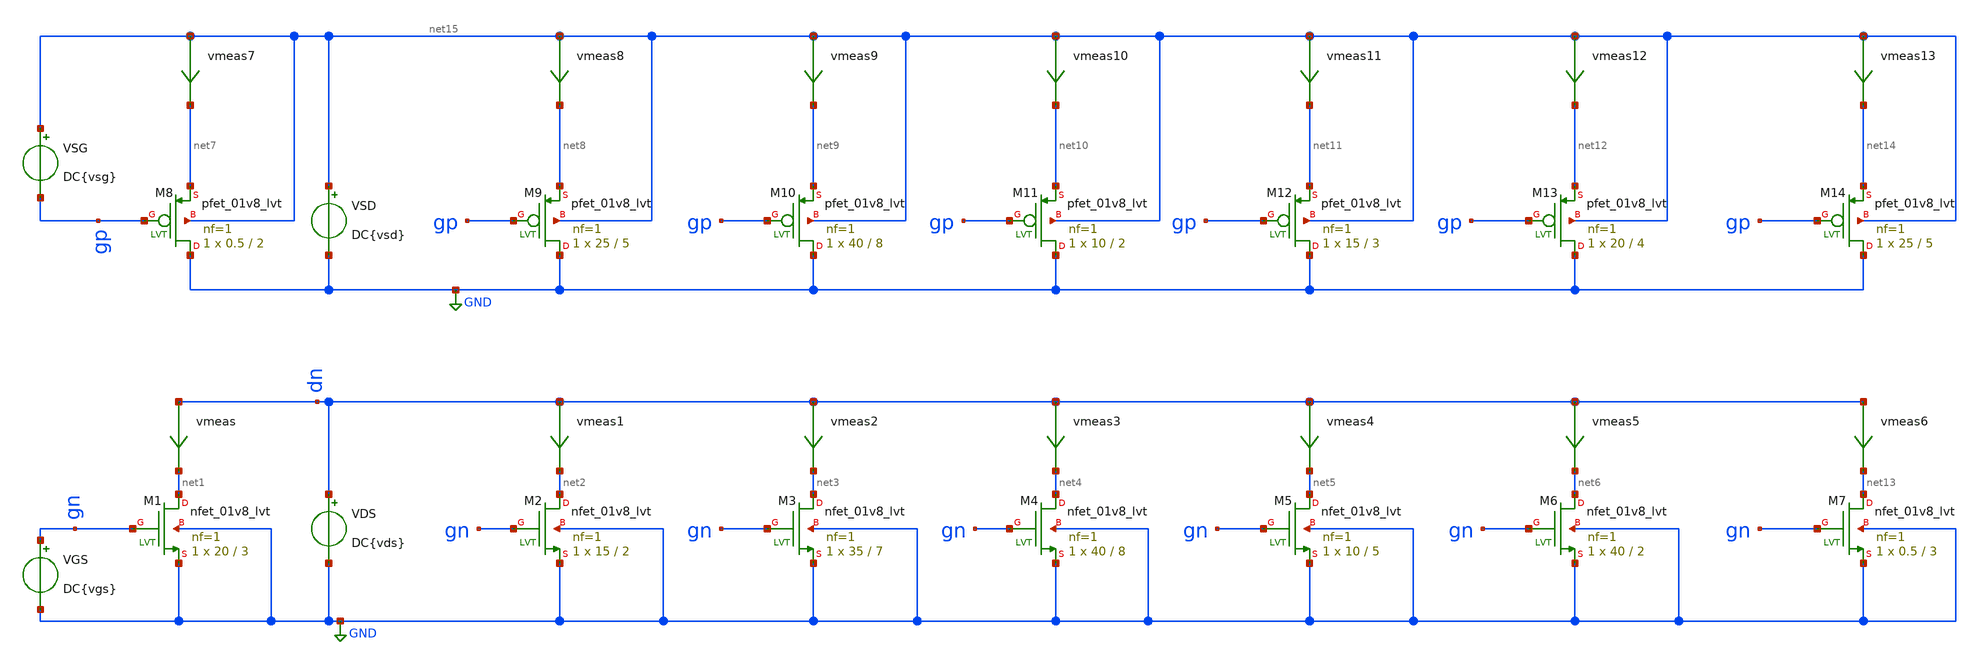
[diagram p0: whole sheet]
** sch_path: XSCHEM/r0_characterization_lvt_01v8.sch
**.subckt r0_characterization_lvt_01v8
XM1 net1 gn GND GND sky130_fd_pr__nfet_01v8_lvt L=3 W=20 nf=1 ad='int((nf+1)/2) * W/nf * 0.29' as='int((nf+2)/2) * W/nf * 0.29'
+ pd='2*int((nf+1)/2) * (W/nf + 0.29)' ps='2*int((nf+2)/2) * (W/nf + 0.29)' nrd='0.29 / W' nrs='0.29 / W'
+ sa=0 sb=0 sd=0 mult=1 m=1
XM2 net2 gn GND GND sky130_fd_pr__nfet_01v8_lvt L=2 W=15 nf=1 ad='int((nf+1)/2) * W/nf * 0.29' as='int((nf+2)/2) * W/nf * 0.29'
+ pd='2*int((nf+1)/2) * (W/nf + 0.29)' ps='2*int((nf+2)/2) * (W/nf + 0.29)' nrd='0.29 / W' nrs='0.29 / W'
+ sa=0 sb=0 sd=0 mult=1 m=1
VGS gn GND DC{vgs}
VDS dn GND DC{vds}
XM3 net3 gn GND GND sky130_fd_pr__nfet_01v8_lvt L=7 W=35 nf=1 ad='int((nf+1)/2) * W/nf * 0.29' as='int((nf+2)/2) * W/nf * 0.29'
+ pd='2*int((nf+1)/2) * (W/nf + 0.29)' ps='2*int((nf+2)/2) * (W/nf + 0.29)' nrd='0.29 / W' nrs='0.29 / W'
+ sa=0 sb=0 sd=0 mult=1 m=1
XM4 net4 gn GND GND sky130_fd_pr__nfet_01v8_lvt L=8 W=40 nf=1 ad='int((nf+1)/2) * W/nf * 0.29' as='int((nf+2)/2) * W/nf * 0.29'
+ pd='2*int((nf+1)/2) * (W/nf + 0.29)' ps='2*int((nf+2)/2) * (W/nf + 0.29)' nrd='0.29 / W' nrs='0.29 / W'
+ sa=0 sb=0 sd=0 mult=1 m=1
XM5 net5 gn GND GND sky130_fd_pr__nfet_01v8_lvt L=5 W=10 nf=1 ad='int((nf+1)/2) * W/nf * 0.29' as='int((nf+2)/2) * W/nf * 0.29'
+ pd='2*int((nf+1)/2) * (W/nf + 0.29)' ps='2*int((nf+2)/2) * (W/nf + 0.29)' nrd='0.29 / W' nrs='0.29 / W'
+ sa=0 sb=0 sd=0 mult=1 m=1
XM6 net6 gn GND GND sky130_fd_pr__nfet_01v8_lvt L=2 W=40 nf=1 ad='int((nf+1)/2) * W/nf * 0.29' as='int((nf+2)/2) * W/nf * 0.29'
+ pd='2*int((nf+1)/2) * (W/nf + 0.29)' ps='2*int((nf+2)/2) * (W/nf + 0.29)' nrd='0.29 / W' nrs='0.29 / W'
+ sa=0 sb=0 sd=0 mult=1 m=1
VSG net15 gp DC{vsg}
VSD net15 GND DC{vsd}
XM7 net13 gn GND GND sky130_fd_pr__nfet_01v8_lvt L=3 W=0.5 nf=1 ad='int((nf+1)/2) * W/nf * 0.29' as='int((nf+2)/2) * W/nf * 0.29'
+ pd='2*int((nf+1)/2) * (W/nf + 0.29)' ps='2*int((nf+2)/2) * (W/nf + 0.29)' nrd='0.29 / W' nrs='0.29 / W'
+ sa=0 sb=0 sd=0 mult=1 m=1
XM8 GND gp net7 net15 sky130_fd_pr__pfet_01v8_lvt L=2 W=0.5 nf=1 ad='int((nf+1)/2) * W/nf * 0.29' as='int((nf+2)/2) * W/nf * 0.29'
+ pd='2*int((nf+1)/2) * (W/nf + 0.29)' ps='2*int((nf+2)/2) * (W/nf + 0.29)' nrd='0.29 / W' nrs='0.29 / W'
+ sa=0 sb=0 sd=0 mult=1 m=1
XM9 GND gp net8 net15 sky130_fd_pr__pfet_01v8_lvt L=5 W=25 nf=1 ad='int((nf+1)/2) * W/nf * 0.29' as='int((nf+2)/2) * W/nf * 0.29'
+ pd='2*int((nf+1)/2) * (W/nf + 0.29)' ps='2*int((nf+2)/2) * (W/nf + 0.29)' nrd='0.29 / W' nrs='0.29 / W'
+ sa=0 sb=0 sd=0 mult=1 m=1
XM10 GND gp net9 net15 sky130_fd_pr__pfet_01v8_lvt L=8 W=40 nf=1 ad='int((nf+1)/2) * W/nf * 0.29' as='int((nf+2)/2) * W/nf * 0.29'
+ pd='2*int((nf+1)/2) * (W/nf + 0.29)' ps='2*int((nf+2)/2) * (W/nf + 0.29)' nrd='0.29 / W' nrs='0.29 / W'
+ sa=0 sb=0 sd=0 mult=1 m=1
XM11 GND gp net10 net15 sky130_fd_pr__pfet_01v8_lvt L=2 W=10 nf=1 ad='int((nf+1)/2) * W/nf * 0.29' as='int((nf+2)/2) * W/nf * 0.29'
+ pd='2*int((nf+1)/2) * (W/nf + 0.29)' ps='2*int((nf+2)/2) * (W/nf + 0.29)' nrd='0.29 / W' nrs='0.29 / W'
+ sa=0 sb=0 sd=0 mult=1 m=1
XM12 GND gp net11 net15 sky130_fd_pr__pfet_01v8_lvt L=3 W=15 nf=1 ad='int((nf+1)/2) * W/nf * 0.29' as='int((nf+2)/2) * W/nf * 0.29'
+ pd='2*int((nf+1)/2) * (W/nf + 0.29)' ps='2*int((nf+2)/2) * (W/nf + 0.29)' nrd='0.29 / W' nrs='0.29 / W'
+ sa=0 sb=0 sd=0 mult=1 m=1
XM13 GND gp net12 net15 sky130_fd_pr__pfet_01v8_lvt L=4 W=20 nf=1 ad='int((nf+1)/2) * W/nf * 0.29' as='int((nf+2)/2) * W/nf * 0.29'
+ pd='2*int((nf+1)/2) * (W/nf + 0.29)' ps='2*int((nf+2)/2) * (W/nf + 0.29)' nrd='0.29 / W' nrs='0.29 / W'
+ sa=0 sb=0 sd=0 mult=1 m=1
XM14 GND gp net14 net15 sky130_fd_pr__pfet_01v8_lvt L=5 W=25 nf=1 ad='int((nf+1)/2) * W/nf * 0.29' as='int((nf+2)/2) * W/nf * 0.29'
+ pd='2*int((nf+1)/2) * (W/nf + 0.29)' ps='2*int((nf+2)/2) * (W/nf + 0.29)' nrd='0.29 / W' nrs='0.29 / W'
+ sa=0 sb=0 sd=0 mult=1 m=1
vmeas dn net1 0
.save i(vmeas)
vmeas1 dn net2 0
.save i(vmeas1)
vmeas2 dn net3 0
.save i(vmeas2)
vmeas3 dn net4 0
.save i(vmeas3)
vmeas4 dn net5 0
.save i(vmeas4)
vmeas5 dn net6 0
.save i(vmeas5)
vmeas6 dn net13 0
.save i(vmeas6)
vmeas7 net15 net7 0
.save i(vmeas7)
vmeas8 net15 net8 0
.save i(vmeas8)
vmeas9 net15 net9 0
.save i(vmeas9)
vmeas10 net15 net10 0
.save i(vmeas10)
vmeas11 net15 net11 0
.save i(vmeas11)
vmeas12 net15 net12 0
.save i(vmeas12)
vmeas13 net15 net14 0
.save i(vmeas13)
**** begin user architecture code



* Parameters
.param vds = 1.8
.param vgs = 0.9
.param vsd = 1.8
.param vsg = 0.9
.options TEMPS = 27.0

* Models
.lib /home/karlajcm/skywater130/skywater-pdk/libraries/sky130_fd_pr/latest/models/sky130.lib.spice TT

* Data to save
.save all  @M.XM1.msky130_fd_pr__nfet_01v8_lvt[id]  @M.XM1.msky130_fd_pr__nfet_01v8_lvt[gm]  @M.XM1.msky130_fd_pr__nfet_01v8_lvt[vth]  @M.XM1.msky130_fd_pr__nfet_01v8_lvt[vds]  @M.XM1.msky130_fd_pr__nfet_01v8_lvt[vdsat]  @M.XM1.msky130_fd_pr__nfet_01v8_lvt[vgs]  @M.XM1.msky130_fd_pr__nfet_01v8_lvt[cgg]  @M.XM2.msky130_fd_pr__nfet_01v8_lvt[id]  @M.XM2.msky130_fd_pr__nfet_01v8_lvt[gm]  @M.XM2.msky130_fd_pr__nfet_01v8_lvt[vth]  @M.XM2.msky130_fd_pr__nfet_01v8_lvt[vds]  @M.XM2.msky130_fd_pr__nfet_01v8_lvt[vdsat]  @M.XM2.msky130_fd_pr__nfet_01v8_lvt[vgs]  @M.XM2.msky130_fd_pr__nfet_01v8_lvt[cgg]  @M.XM3.msky130_fd_pr__nfet_01v8_lvt[id]  @M.XM3.msky130_fd_pr__nfet_01v8_lvt[gm]  @M.XM3.msky130_fd_pr__nfet_01v8_lvt[vth]  @M.XM3.msky130_fd_pr__nfet_01v8_lvt[vds]  @M.XM3.msky130_fd_pr__nfet_01v8_lvt[vdsat]  @M.XM3.msky130_fd_pr__nfet_01v8_lvt[vgs]  @M.XM3.msky130_fd_pr__nfet_01v8_lvt[cgg]  @M.XM4.msky130_fd_pr__nfet_01v8_lvt[id]  @M.XM4.msky130_fd_pr__nfet_01v8_lvt[gm]  @M.XM4.msky130_fd_pr__nfet_01v8_lvt[vth]  @M.XM4.msky130_fd_pr__nfet_01v8_lvt[vds]  @M.XM4.msky130_fd_pr__nfet_01v8_lvt[vdsat]  @M.XM4.msky130_fd_pr__nfet_01v8_lvt[vgs]  @M.XM4.msky130_fd_pr__nfet_01v8_lvt[cgg]  @M.XM5.msky130_fd_pr__nfet_01v8_lvt[id]  @M.XM5.msky130_fd_pr__nfet_01v8_lvt[gm]  @M.XM5.msky130_fd_pr__nfet_01v8_lvt[vth]  @M.XM5.msky130_fd_pr__nfet_01v8_lvt[vds]  @M.XM5.msky130_fd_pr__nfet_01v8_lvt[vdsat]  @M.XM5.msky130_fd_pr__nfet_01v8_lvt[vgs]  @M.XM5.msky130_fd_pr__nfet_01v8_lvt[cgg]  @M.XM6.msky130_fd_pr__nfet_01v8_lvt[id]  @M.XM6.msky130_fd_pr__nfet_01v8_lvt[gm]  @M.XM6.msky130_fd_pr__nfet_01v8_lvt[vth]  @M.XM6.msky130_fd_pr__nfet_01v8_lvt[vds]  @M.XM6.msky130_fd_pr__nfet_01v8_lvt[vdsat]  @M.XM6.msky130_fd_pr__nfet_01v8_lvt[vgs]  @M.XM6.msky130_fd_pr__nfet_01v8_lvt[cgg]  @M.XM7.msky130_fd_pr__nfet_01v8_lvt[id]  @M.XM7.msky130_fd_pr__nfet_01v8_lvt[gm]  @M.XM7.msky130_fd_pr__nfet_01v8_lvt[vth]  @M.XM7.msky130_fd_pr__nfet_01v8_lvt[vds]  @M.XM7.msky130_fd_pr__nfet_01v8_lvt[vdsat]  @M.XM7.msky130_fd_pr__nfet_01v8_lvt[vgs]  @M.XM7.msky130_fd_pr__nfet_01v8_lvt[cgg]  @M.XM8.msky130_fd_pr__pfet_01v8_lvt[id]  @M.XM8.msky130_fd_pr__pfet_01v8_lvt[gm]  @M.XM8.msky130_fd_pr__pfet_01v8_lvt[vth]  @M.XM8.msky130_fd_pr__pfet_01v8_lvt[vds]  @M.XM8.msky130_fd_pr__pfet_01v8_lvt[vdsat]  @M.XM8.msky130_fd_pr__pfet_01v8_lvt[vgs]  @M.XM8.msky130_fd_pr__pfet_01v8_lvt[cgg]  @M.XM9.msky130_fd_pr__pfet_01v8_lvt[id]  @M.XM9.msky130_fd_pr__pfet_01v8_lvt[gm]  @M.XM9.msky130_fd_pr__pfet_01v8_lvt[vth]  @M.XM9.msky130_fd_pr__pfet_01v8_lvt[vds]  @M.XM9.msky130_fd_pr__pfet_01v8_lvt[vdsat]  @M.XM9.msky130_fd_pr__pfet_01v8_lvt[vgs]  @M.XM9.msky130_fd_pr__pfet_01v8_lvt[cgg]  @M.XM10.msky130_fd_pr__pfet_01v8_lvt[id]  @M.XM10.msky130_fd_pr__pfet_01v8_lvt[gm]  @M.XM10.msky130_fd_pr__pfet_01v8_lvt[vth]  @M.XM10.msky130_fd_pr__pfet_01v8_lvt[vds]  @M.XM10.msky130_fd_pr__pfet_01v8_lvt[vdsat]  @M.XM10.msky130_fd_pr__pfet_01v8_lvt[vgs]  @M.XM10.msky130_fd_pr__pfet_01v8_lvt[cgg]  @M.XM11.msky130_fd_pr__pfet_01v8_lvt[id]  @M.XM11.msky130_fd_pr__pfet_01v8_lvt[gm]  @M.XM11.msky130_fd_pr__pfet_01v8_lvt[vth]  @M.XM11.msky130_fd_pr__pfet_01v8_lvt[vds]  @M.XM11.msky130_fd_pr__pfet_01v8_lvt[vdsat]  @M.XM11.msky130_fd_pr__pfet_01v8_lvt[vgs]  @M.XM11.msky130_fd_pr__pfet_01v8_lvt[cgg]  @M.XM12.msky130_fd_pr__pfet_01v8_lvt[id]  @M.XM12.msky130_fd_pr__pfet_01v8_lvt[gm]  @M.XM12.msky130_fd_pr__pfet_01v8_lvt[vth]  @M.XM12.msky130_fd_pr__pfet_01v8_lvt[vds]  @M.XM12.msky130_fd_pr__pfet_01v8_lvt[vdsat]  @M.XM12.msky130_fd_pr__pfet_01v8_lvt[vgs]  @M.XM12.msky130_fd_pr__pfet_01v8_lvt[cgg]  @M.XM13.msky130_fd_pr__pfet_01v8_lvt[id]  @M.XM13.msky130_fd_pr__pfet_01v8_lvt[gm]  @M.XM13.msky130_fd_pr__pfet_01v8_lvt[vth]  @M.XM13.msky130_fd_pr__pfet_01v8_lvt[vds]  @M.XM13.msky130_fd_pr__pfet_01v8_lvt[vdsat]  @M.XM13.msky130_fd_pr__pfet_01v8_lvt[vgs]  @M.XM13.msky130_fd_pr__pfet_01v8_lvt[cgg]  @M.XM14.msky130_fd_pr__pfet_01v8_lvt[id]  @M.XM14.msky130_fd_pr__pfet_01v8_lvt[gm]  @M.XM14.msky130_fd_pr__pfet_01v8_lvt[vth]  @M.XM14.msky130_fd_pr__pfet_01v8_lvt[vds]  @M.XM14.msky130_fd_pr__pfet_01v8_lvt[vdsat]  @M.XM14.msky130_fd_pr__pfet_01v8_lvt[vgs]  @M.XM14.msky130_fd_pr__pfet_01v8_lvt[cgg]

* Simulation
.control
  dc VDS 0 1.8 0.01 VGS 0 1.8 0.3 VSD 0 1.8 0.01 VSG 0 1.8 0.3
  setplot dc1
  plot @M.XM1.msky130_fd_pr__nfet_01v8_lvt[id] @M.XM2.msky130_fd_pr__nfet_01v8_lvt[id] @M.XM3.msky130_fd_pr__nfet_01v8_lvt[id]
+ @M.XM4.msky130_fd_pr__nfet_01v8_lvt[id] @M.XM5.msky130_fd_pr__nfet_01v8_lvt[id] @M.XM6.msky130_fd_pr__nfet_01v8_lvt[id]
+ @M.XM7.msky130_fd_pr__nfet_01v8_lvt[id] ylabel Id xlabel Vds title 'NMOS: Id vs Vds vs Vgs'
  plot @M.XM8.msky130_fd_pr__pfet_01v8_lvt[id] @M.XM9.msky130_fd_pr__pfet_01v8_lvt[id] @M.XM10.msky130_fd_pr__pfet_01v8_lvt[id]
+ @M.XM11.msky130_fd_pr__pfet_01v8_lvt[id] @M.XM12.msky130_fd_pr__pfet_01v8_lvt[id] @M.XM13.msky130_fd_pr__pfet_01v8_lvt[id]
+ @M.XM14.msky130_fd_pr__pfet_01v8_lvt[id] ylabel Id xlabel Vsd title 'PMOS:Id vs Vsd vs Vsg'
  set filetype = ascii
  write r0_characterization_lvt_01v8_dc1.raw

  reset
  dc VDS 0 1.8 0.01
  setplot dc2
  plot i(vmeas) ylabel Ids xlabel Vds title 'M1:NMOS:Ids vs Vds'
  plot i(vmeas1) ylabel Ids xlabel Vds title 'M2:NMOS:Ids vs Vds'
  plot i(vmeas2) ylabel Ids xlabel Vds title 'M3:NMOS:Ids vs Vds'
  plot i(vmeas3) ylabel Ids xlabel Vds title 'M4:NMOS:Ids vs Vds'
  plot i(vmeas4) ylabel Ids xlabel Vds title 'M5:NMOS:Ids vs Vds'
  plot i(vmeas5) ylabel Ids xlabel Vds title 'M6:NMOS:Ids vs Vds'
  plot i(vmeas6) ylabel Ids xlabel Vds title 'M7:NMOS:Ids vs Vds'
  set filetype = ascii
  write r0_characterization_lvt_01v8_dc2.raw

  reset
  dc VSD 0 1.8 0.01
  setplot dc3
  plot i(vmeas7) ylabel Ids xlabel Vds title 'M8:PMOS:Isd vs Vsd'
  plot i(vmeas8) ylabel Ids xlabel Vds title 'M9:PMOS:Isd vs Vsd'
  plot i(vmeas9) ylabel Ids xlabel Vds title 'M10:PMOS:Isd vs Vsd'
  plot i(vmeas10) ylabel Ids xlabel Vds title 'M11:PMOS:Isd vs Vsd'
  plot i(vmeas11) ylabel Ids xlabel Vds title 'M12:PMOS:Isd vs Vsd'
  plot i(vmeas12) ylabel Ids xlabel Vds title 'M13:PMOS:Isd vs Vsd'
  plot i(vmeas13) ylabel Ids xlabel Vds title 'M14:PMOS:Isd vs Vsd'
  set filetype = ascii
  write r0_characterization_lvt_01v8_dc3.raw

  *alterparam vds = 0
  *alterparam vsd = 0
  *reset
  *dc VGS -1.8 1.8 0.01 VSG -1.8 1.8 0.01
  *setplot dc2
  *plot @M.XM1.msky130_fd_pr__nfet_01v8_lvt[cgg] @M.XM2.msky130_fd_pr__nfet_01v8_lvt[cgg] @M.XM3.msky130_fd_pr__nfet_01v8_lvt[cgg]
+ @M.XM4.msky130_fd_pr__nfet_01v8_lvt[cgg] @M.XM5.msky130_fd_pr__nfet_01v8_lvt[cgg] @M.XM6.msky130_fd_pr__nfet_01v8_lvt[cgg]
+ @M.XM7.msky130_fd_pr__nfet_01v8_lvt[cgg] ylabel Cgg xlabel Vgs title 'NMOS:Cgg vs Vgs'
  *plot @M.XM8.msky130_fd_pr__pfet_01v8_lvt[cgg] @M.XM9.msky130_fd_pr__pfet_01v8_lvt[cgg] @M.XM10.msky130_fd_pr__pfet_01v8_lvt[cgg]
+ @M.XM11.msky130_fd_pr__pfet_01v8_lvt[cgg] @M.XM12.msky130_fd_pr__pfet_01v8_lvt[cgg] @M.XM13.msky130_fd_pr__pfet_01v8_lvt[cgg]
+ @M.XM14.msky130_fd_pr__pfet_01v8_lvt[cgg] ylabel Cgg xlabel Vgs title 'PMOS:Cgg vs Vsg'
  *set filetype = ascii
  *write r0_characterization_lvt_01v8_dc2.raw

  *reset
  *dc VGS -1.8 1.8 0.01 VSG -1.8 1.8 0.01
  *setplot dc3
  *plot @M.XM1.msky130_fd_pr__nfet_01v8_lvt[vth] @M.XM2.msky130_fd_pr__nfet_01v8_lvt[vth] @M.XM3.msky130_fd_pr__nfet_01v8_lvt[vth]
+ @M.XM4.msky130_fd_pr__nfet_01v8_lvt[vth] @M.XM5.msky130_fd_pr__nfet_01v8_lvt[vth] @M.XM6.msky130_fd_pr__nfet_01v8_lvt[vth]
+ @M.XM7.msky130_fd_pr__nfet_01v8_lvt[vth] ylabel Vth xlabel Vgs title 'NMOS:Vth vs Vgs'
  *plot @M.XM8.msky130_fd_pr__pfet_01v8_lvt[vth] @M.XM9.msky130_fd_pr__pfet_01v8_lvt[vth] @M.XM10.msky130_fd_pr__pfet_01v8_lvt[vth]
+ @M.XM11.msky130_fd_pr__pfet_01v8_lvt[vth] @M.XM12.msky130_fd_pr__pfet_01v8_lvt[vth] @M.XM13.msky130_fd_pr__pfet_01v8_lvt[vth]
+ @M.XM14.msky130_fd_pr__pfet_01v8_lvt[vth] ylabel Vth xlabel Vsg title 'PMOS:Vth vs Vsg'
  *set filetype = ascii
  *write r0_characterization_lvt_01v8_dc3.raw

  reset
  unset filetype
  op
  save all
  write r0_characterization_lvt_01v8.raw

.endc

.end


**** end user architecture code
**.ends
.GLOBAL GND
.end
